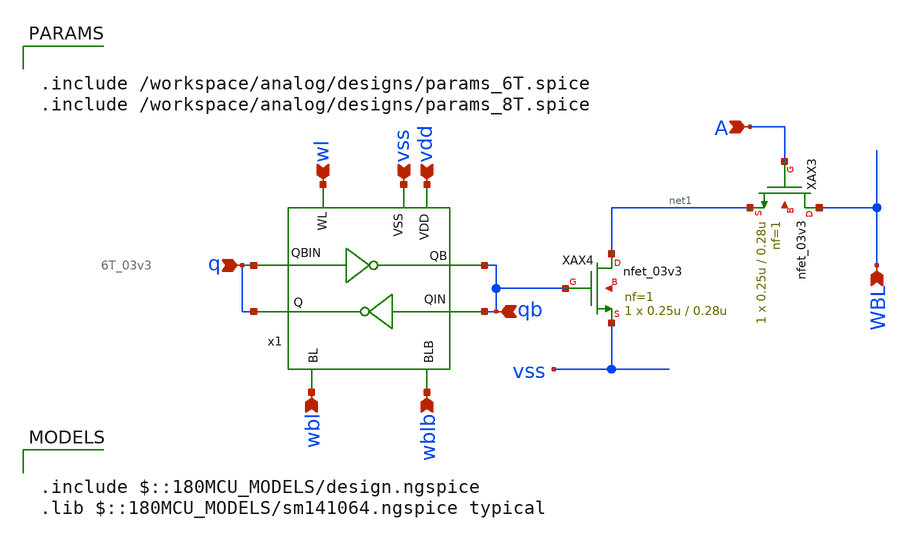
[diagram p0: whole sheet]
** sch_path: analog/designs/8T_03v3.sch
**.subckt 8T_03v3 A WBL qb q wl vss vdd wblb wbl
*.ipin A
*.ipin WBL
*.ipin qb
*.ipin q
*.ipin wl
*.ipin vss
*.ipin vdd
*.ipin wblb
*.ipin wbl
XAX4 net1 qb vss net2 nfet_03v3 L=0.28u W=0.25u nf=1 ad='int((nf+1)/2) * W/nf * 0.18u' as='int((nf+2)/2) * W/nf * 0.18u'
+ pd='2*int((nf+1)/2) * (W/nf + 0.18u)' ps='2*int((nf+2)/2) * (W/nf + 0.18u)' nrd='0.18u / W' nrs='0.18u / W'
+ sa=0 sb=0 sd=0 m=1
XAX3 WBL A net1 net3 nfet_03v3 L=0.28u W=0.25u nf=1 ad='int((nf+1)/2) * W/nf * 0.18u' as='int((nf+2)/2) * W/nf * 0.18u'
+ pd='2*int((nf+1)/2) * (W/nf + 0.18u)' ps='2*int((nf+2)/2) * (W/nf + 0.18u)' nrd='0.18u / W' nrs='0.18u / W'
+ sa=0 sb=0 sd=0 m=1
x1 wl vdd wbl wblb qb qb q vss q 6T_03v3
**** begin user architecture code

.include /workspace/analog/designs/params_6T.spice
.include /workspace/analog/designs/params_8T.spice


.include $::180MCU_MODELS/design.ngspice
.lib $::180MCU_MODELS/sm141064.ngspice typical

**** end user architecture code
**.ends

* expanding   symbol:  analog/designs/6T_03v3.sym # of pins=9
** sym_path: analog/designs/6T_03v3.sym
** sch_path: analog/designs/6T_03v3.sch
.subckt 6T_03v3 WL VDD BL BLB QIN QB QBIN VSS Q
*.ipin VSS
*.ipin VDD
*.ipin WL
*.ipin BL
*.ipin BLB
*.ipin QBIN
*.ipin QIN
*.opin Q
*.opin QB
XPD1 QB QBIN VSS VSS nfet_03v3 L='L_PD' W='W_PD' nf=1 ad='int((nf+1)/2) * W/nf * 0.18u' as='int((nf+2)/2) * W/nf * 0.18u'
+ pd='2*int((nf+1)/2) * (W/nf + 0.18u)' ps='2*int((nf+2)/2) * (W/nf + 0.18u)' nrd='0.18u / W' nrs='0.18u / W'
+ sa=0 sb=0 sd=0 m=1
XPU1 QB QBIN VDD VDD pfet_03v3 L='L_PU' W='W_PU' nf=1 ad='int((nf+1)/2) * W/nf * 0.18u' as='int((nf+2)/2) * W/nf * 0.18u'
+ pd='2*int((nf+1)/2) * (W/nf + 0.18u)' ps='2*int((nf+2)/2) * (W/nf + 0.18u)' nrd='0.18u / W' nrs='0.18u / W'
+ sa=0 sb=0 sd=0 m=1
XAX1 BLB WL QB VSS nfet_03v3 L='W_AX' W='L_AX' nf=1 ad='int((nf+1)/2) * W/nf * 0.18u' as='int((nf+2)/2) * W/nf * 0.18u'
+ pd='2*int((nf+1)/2) * (W/nf + 0.18u)' ps='2*int((nf+2)/2) * (W/nf + 0.18u)' nrd='0.18u / W' nrs='0.18u / W'
+ sa=0 sb=0 sd=0 m=1
XPU2 Q QIN VDD VDD pfet_03v3 L='L_PU' W='W_PU' nf=1 ad='int((nf+1)/2) * W/nf * 0.18u' as='int((nf+2)/2) * W/nf * 0.18u'
+ pd='2*int((nf+1)/2) * (W/nf + 0.18u)' ps='2*int((nf+2)/2) * (W/nf + 0.18u)' nrd='0.18u / W' nrs='0.18u / W'
+ sa=0 sb=0 sd=0 m=1
XPD2 Q QIN VSS VSS nfet_03v3 L='L_PD' W='W_PD' nf=1 ad='int((nf+1)/2) * W/nf * 0.18u' as='int((nf+2)/2) * W/nf * 0.18u'
+ pd='2*int((nf+1)/2) * (W/nf + 0.18u)' ps='2*int((nf+2)/2) * (W/nf + 0.18u)' nrd='0.18u / W' nrs='0.18u / W'
+ sa=0 sb=0 sd=0 m=1
XAX2 BL WL Q VSS nfet_03v3 L='W_AX' W='L_AX' nf=1 ad='int((nf+1)/2) * W/nf * 0.18u' as='int((nf+2)/2) * W/nf * 0.18u'
+ pd='2*int((nf+1)/2) * (W/nf + 0.18u)' ps='2*int((nf+2)/2) * (W/nf + 0.18u)' nrd='0.18u / W' nrs='0.18u / W'
+ sa=0 sb=0 sd=0 m=1
.ends

.end
